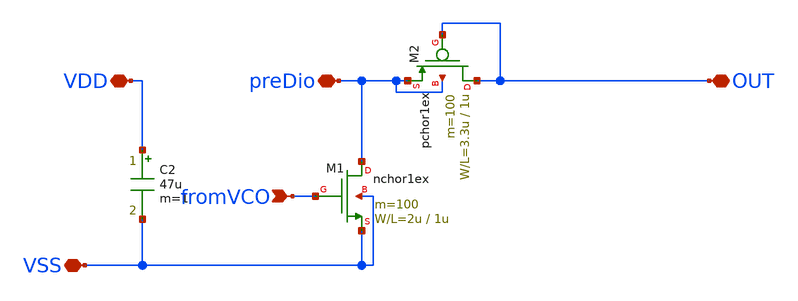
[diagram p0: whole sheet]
** sch_path: design/xschem/sebasu_TOP.sch.sch
**.subckt sebasu_TOP.sch VDD fromVCO preDio VSS OUT
*.iopin VDD
*.ipin fromVCO
*.iopin preDio
*.iopin VSS
*.iopin OUT
M1 preDio fromVCO VSS VSS nchor1ex L=1u W=2u m=100
M2 OUT OUT preDio preDio pchor1ex L=1u W=3.3u m=100
C2 VDD VSS 47u m=1
**.ends
.end
